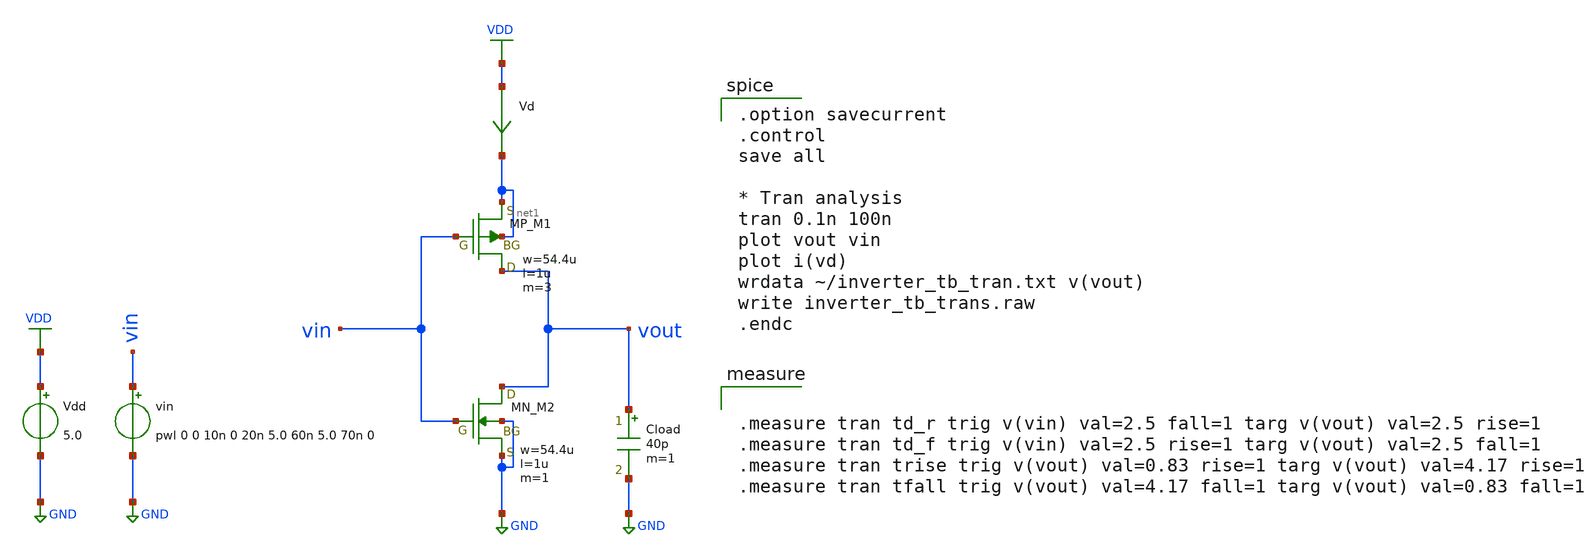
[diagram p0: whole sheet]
** sch_path: member_project/inverter/RISE-A/jijinbei/inverter_cap_trans.sch
**.subckt inverter_cap_trans
Vdd VDD GND 5.0
vin vin GND pwl 0 0 10n 0 20n 5.0 60n 5.0 70n 0
Vd VDD net1 0
.save i(vd)
Cload vout GND 40p m=1
XM1 vout vin net1 net1 PMOS w=54.4u l=1u as=0 ad=0 ps=0 pd=0 nrd=0 nrs=0 m=3
XM2 vout vin GND GND NMOS w=54.4u l=1u as=0 ad=0 ps=0 pd=0 nrd=0 nrs=0 m=1
**** begin user architecture code

.option savecurrent
.control
save all

* Tran analysis
tran 0.1n 100n
plot vout vin
plot i(vd)
wrdata ~/inverter_tb_tran.txt v(vout)
write inverter_tb_trans.raw
.endc



.measure tran td_r trig v(vin) val=2.5 fall=1 targ v(vout) val=2.5 rise=1
.measure tran td_f trig v(vin) val=2.5 rise=1 targ v(vout) val=2.5 fall=1
.measure tran trise trig v(vout) val=0.83 rise=1 targ v(vout) val=4.17 rise=1
.measure tran tfall trig v(vout) val=4.17 fall=1 targ v(vout) val=0.83 fall=1


 .include $::LIB/ip62_models
**** end user architecture code
**.ends
.GLOBAL VDD
.GLOBAL GND
.end
